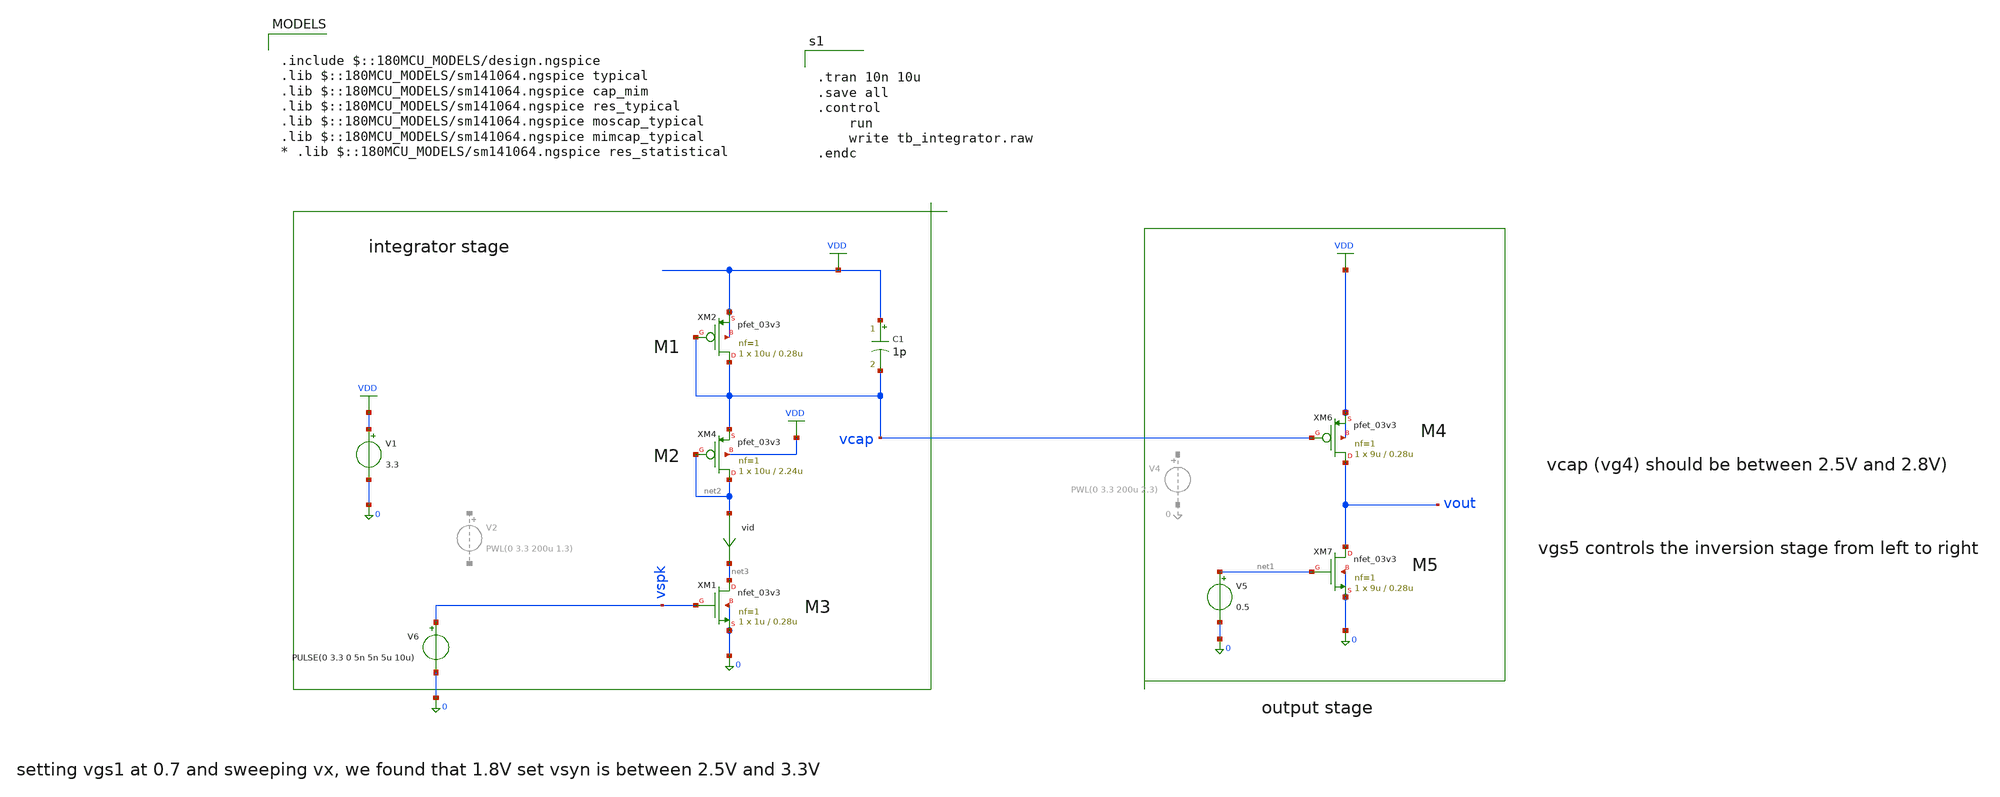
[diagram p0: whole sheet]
** sch_path: designs/libs/snn_analog/sch/integrator/tb_integrator.sch
**.subckt tb_integrator
XM1 net3 vspk 0 0 nfet_03v3 L=0.28u W=1u nf=1 ad='int((nf+1)/2) * W/nf * 0.18u' as='int((nf+2)/2) * W/nf * 0.18u'
+ pd='2*int((nf+1)/2) * (W/nf + 0.18u)' ps='2*int((nf+2)/2) * (W/nf + 0.18u)' nrd='0.18u / W' nrs='0.18u / W'
+ sa=0 sb=0 sd=0 m=1
XM2 vcap vcap VDD VDD pfet_03v3 L=0.28u W=10u nf=1 ad='int((nf+1)/2) * W/nf * 0.18u' as='int((nf+2)/2) * W/nf * 0.18u'
+ pd='2*int((nf+1)/2) * (W/nf + 0.18u)' ps='2*int((nf+2)/2) * (W/nf + 0.18u)' nrd='0.18u / W' nrs='0.18u / W'
+ sa=0 sb=0 sd=0 m=1
XM4 net2 net2 vcap VDD pfet_03v3 L=2.24u W=10u nf=1 ad='int((nf+1)/2) * W/nf * 0.18u' as='int((nf+2)/2) * W/nf * 0.18u'
+ pd='2*int((nf+1)/2) * (W/nf + 0.18u)' ps='2*int((nf+2)/2) * (W/nf + 0.18u)' nrd='0.18u / W' nrs='0.18u / W'
+ sa=0 sb=0 sd=0 m=1
C1 VDD vcap 1p m=1
V1 VDD 0 3.3
XM6 vout vcap VDD VDD pfet_03v3 L=0.28u W=9u nf=1 ad='int((nf+1)/2) * W/nf * 0.18u' as='int((nf+2)/2) * W/nf * 0.18u'
+ pd='2*int((nf+1)/2) * (W/nf + 0.18u)' ps='2*int((nf+2)/2) * (W/nf + 0.18u)' nrd='0.18u / W' nrs='0.18u / W'
+ sa=0 sb=0 sd=0 m=1
XM7 vout net1 0 0 nfet_03v3 L=0.28u W=9u nf=1 ad='int((nf+1)/2) * W/nf * 0.18u' as='int((nf+2)/2) * W/nf * 0.18u'
+ pd='2*int((nf+1)/2) * (W/nf + 0.18u)' ps='2*int((nf+2)/2) * (W/nf + 0.18u)' nrd='0.18u / W' nrs='0.18u / W'
+ sa=0 sb=0 sd=0 m=1
V5 net1 0 0.5
V6 vspk 0 PULSE(0 3.3 0 5n 5n 5u 10u)
vid net2 net3 0
.save i(vid)
**** begin user architecture code

.include $::180MCU_MODELS/design.ngspice
.lib $::180MCU_MODELS/sm141064.ngspice typical
.lib $::180MCU_MODELS/sm141064.ngspice cap_mim
.lib $::180MCU_MODELS/sm141064.ngspice res_typical
.lib $::180MCU_MODELS/sm141064.ngspice moscap_typical
.lib $::180MCU_MODELS/sm141064.ngspice mimcap_typical
* .lib $::180MCU_MODELS/sm141064.ngspice res_statistical



.tran 10n 10u
.save all
.control
	run
	write tb_integrator.raw
.endc


**** end user architecture code
**.ends
.GLOBAL VDD
.end
